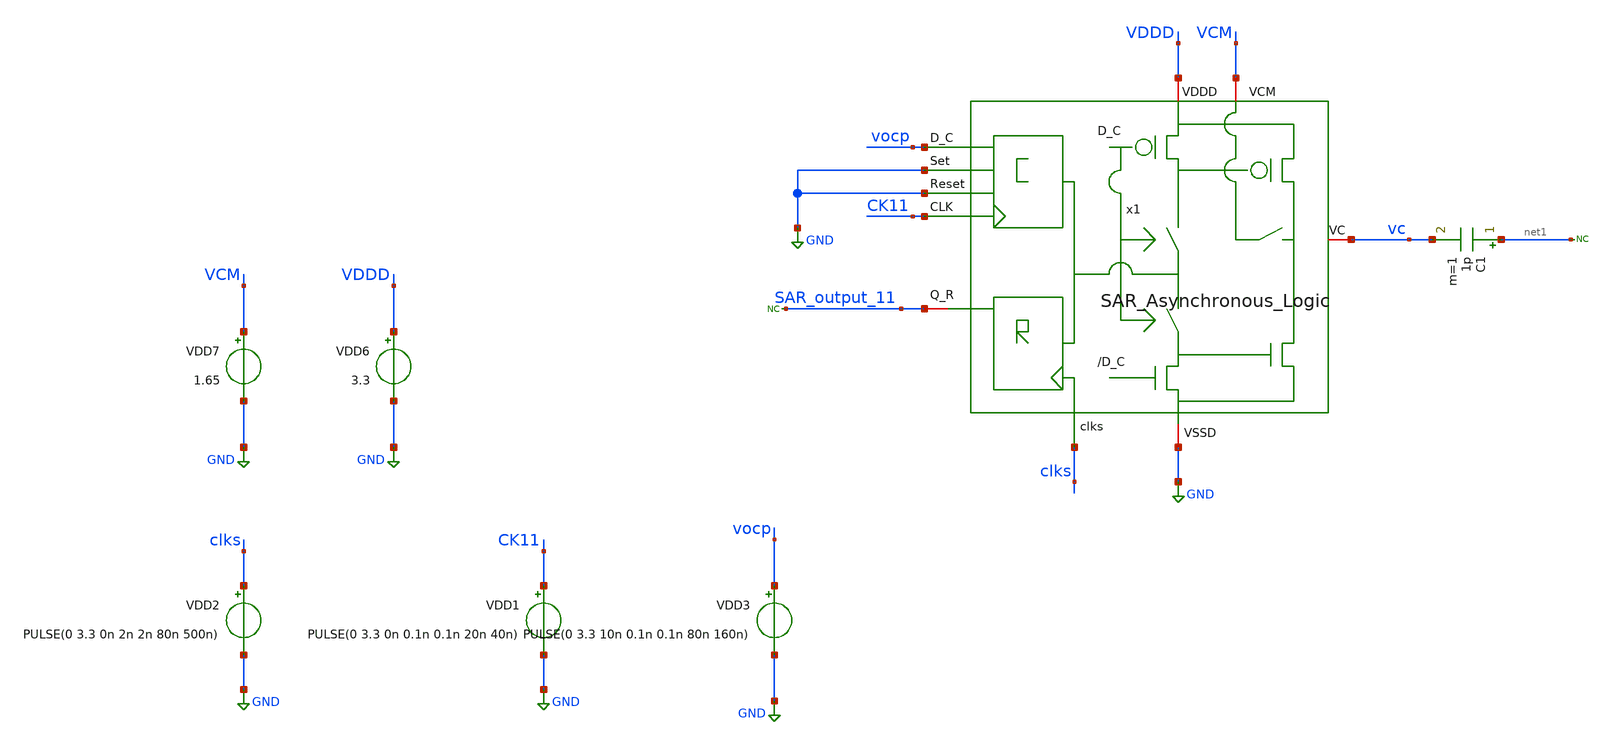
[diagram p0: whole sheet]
** sch_path: SAR_ADC/SAR_Asynchronous_Logic/xschem/SAR_Asynchronous_Logic_tb.sch
**.subckt SAR_Asynchronous_Logic_tb
* noconn #net1
C1 net1 vc 1p m=1
* noconn SAR_output_11
VDD6 VDDD GND 3.3
VDD7 VCM GND 1.65
VDD2 clks GND PULSE(0 3.3 0n 2n 2n 80n 500n)
VDD1 CK11 GND PULSE(0 3.3 0n 0.1n 0.1n 20n 40n)
VDD3 vocp GND PULSE(0 3.3 10n 0.1n 0.1n 80n 160n)
x1 VCM vc SAR_output_11 clks VDDD GND GND GND vocp CK11 SAR_Asynchronous_Logic
**** begin user architecture code



*Parameters

.options TEMP = 50.0
.lib /home/gf180/Documents/gf180/pdk/gf180mcuD/libs.tech/ngspice/sm141064.ngspice typical
.include /home/gf180/Documents/gf180/pdk/gf180mcuD/libs.tech/ngspice/design.ngspice

*Data to save
.save all


* Simulation
.control
tran 0.1n 500n
*setplot dc1
plot V(CK11)+20 V(vocp)+16 V(x2.Dn)+12 V(x2.VA)+8 V(x2.VB)+4 V(vc)
set filetype = ascii
write SAR_Asynchronous_Logic_tb_tran.raw

reset
unset filetype
op
save all
write SAR_Asynchronous_Logic_tb.raw


.endc
.end


**** end user architecture code
**.ends
.GLOBAL GND
.end
